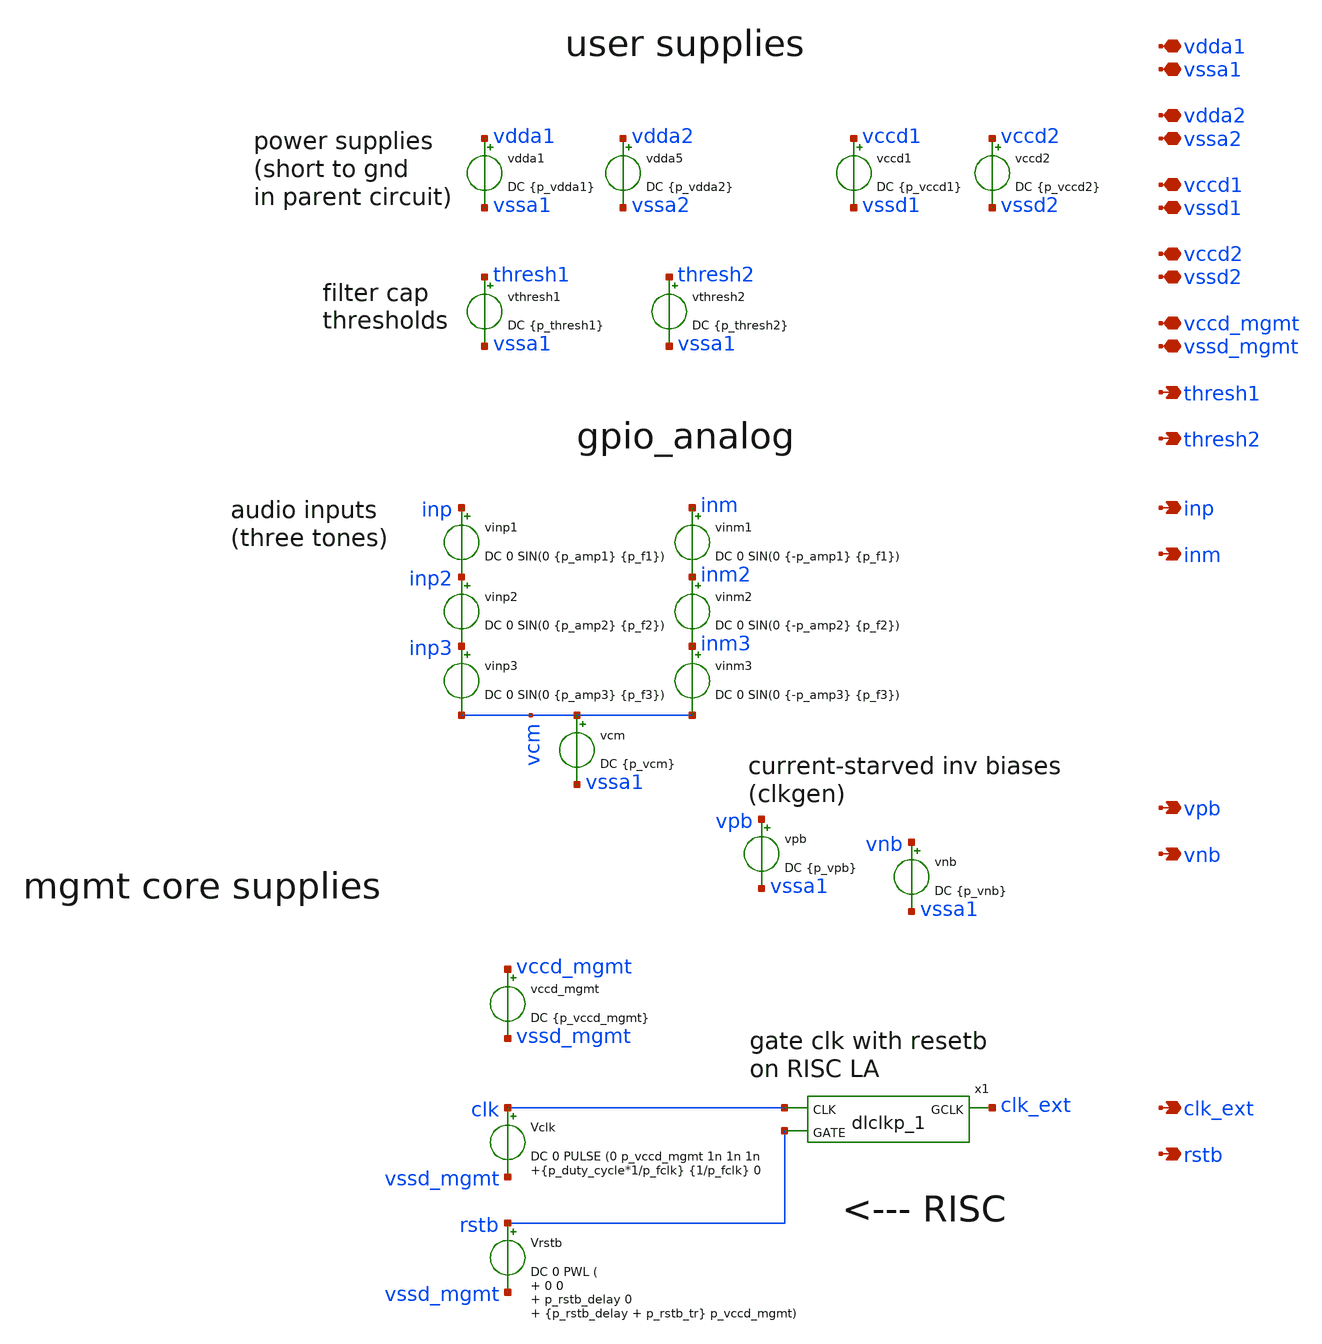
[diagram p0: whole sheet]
** sch_path: xschem/test_bench/pad_frame.sch
**.subckt pad_frame thresh1 thresh2 inp inm rstb clk_ext vpb vnb vccd1 vssd1 vdda1 vssa1 vdda2 vssa2
*+ vccd2 vssd2 vccd_mgmt vssd_mgmt
*.opin thresh1
*.opin thresh2
*.opin inp
*.opin inm
*.opin rstb
*.opin clk_ext
*.opin vpb
*.opin vnb
*.iopin vccd1
*.iopin vssd1
*.iopin vdda1
*.iopin vssa1
*.iopin vdda2
*.iopin vssa2
*.iopin vccd2
*.iopin vssd2
*.iopin vccd_mgmt
*.iopin vssd_mgmt
vdda1 vdda1 vssa1 DC {p_vdda1}
vthresh1 thresh1 vssa1 DC {p_thresh1}
vthresh2 thresh2 vssa1 DC {p_thresh2}
vinp1 inp inp2 DC 0 SIN(0 {p_amp1} {p_f1})
vinm1 inm inm2 DC 0 SIN(0 {-p_amp1} {p_f1})
vpb vpb vssa1 DC {p_vpb}
vnb vnb vssa1 DC {p_vnb}
vinp2 inp2 inp3 DC 0 SIN(0 {p_amp2} {p_f2})
vinp3 inp3 vcm DC 0 SIN(0 {p_amp3} {p_f3})
vinm2 inm2 inm3 DC 0 SIN(0 {-p_amp2} {p_f2})
vinm3 inm3 vcm DC 0 SIN(0 {-p_amp3} {p_f3})
vcm vcm vssa1 DC {p_vcm}
vccd1 vccd1 vssd1 DC {p_vccd1}
Vclk clk vssd_mgmt DC 0 PULSE (0 p_vccd_mgmt 1n 1n 1n {p_duty_cycle*1/p_fclk} {1/p_fclk} 0
Vrstb rstb vssd_mgmt DC 0 PWL ( 0 0 p_rstb_delay 0 {p_rstb_delay + p_rstb_tr} p_vccd_mgmt)
x1 clk rstb vssd_mgmt vssd_mgmt vccd_mgmt vccd_mgmt clk_ext sky130_fd_sc_hd__dlclkp_1
vccd_mgmt vccd_mgmt vssd_mgmt DC {p_vccd_mgmt}
vccd2 vccd2 vssd2 DC {p_vccd2}
vdda5 vdda2 vssa2 DC {p_vdda2}
**.ends
.end
